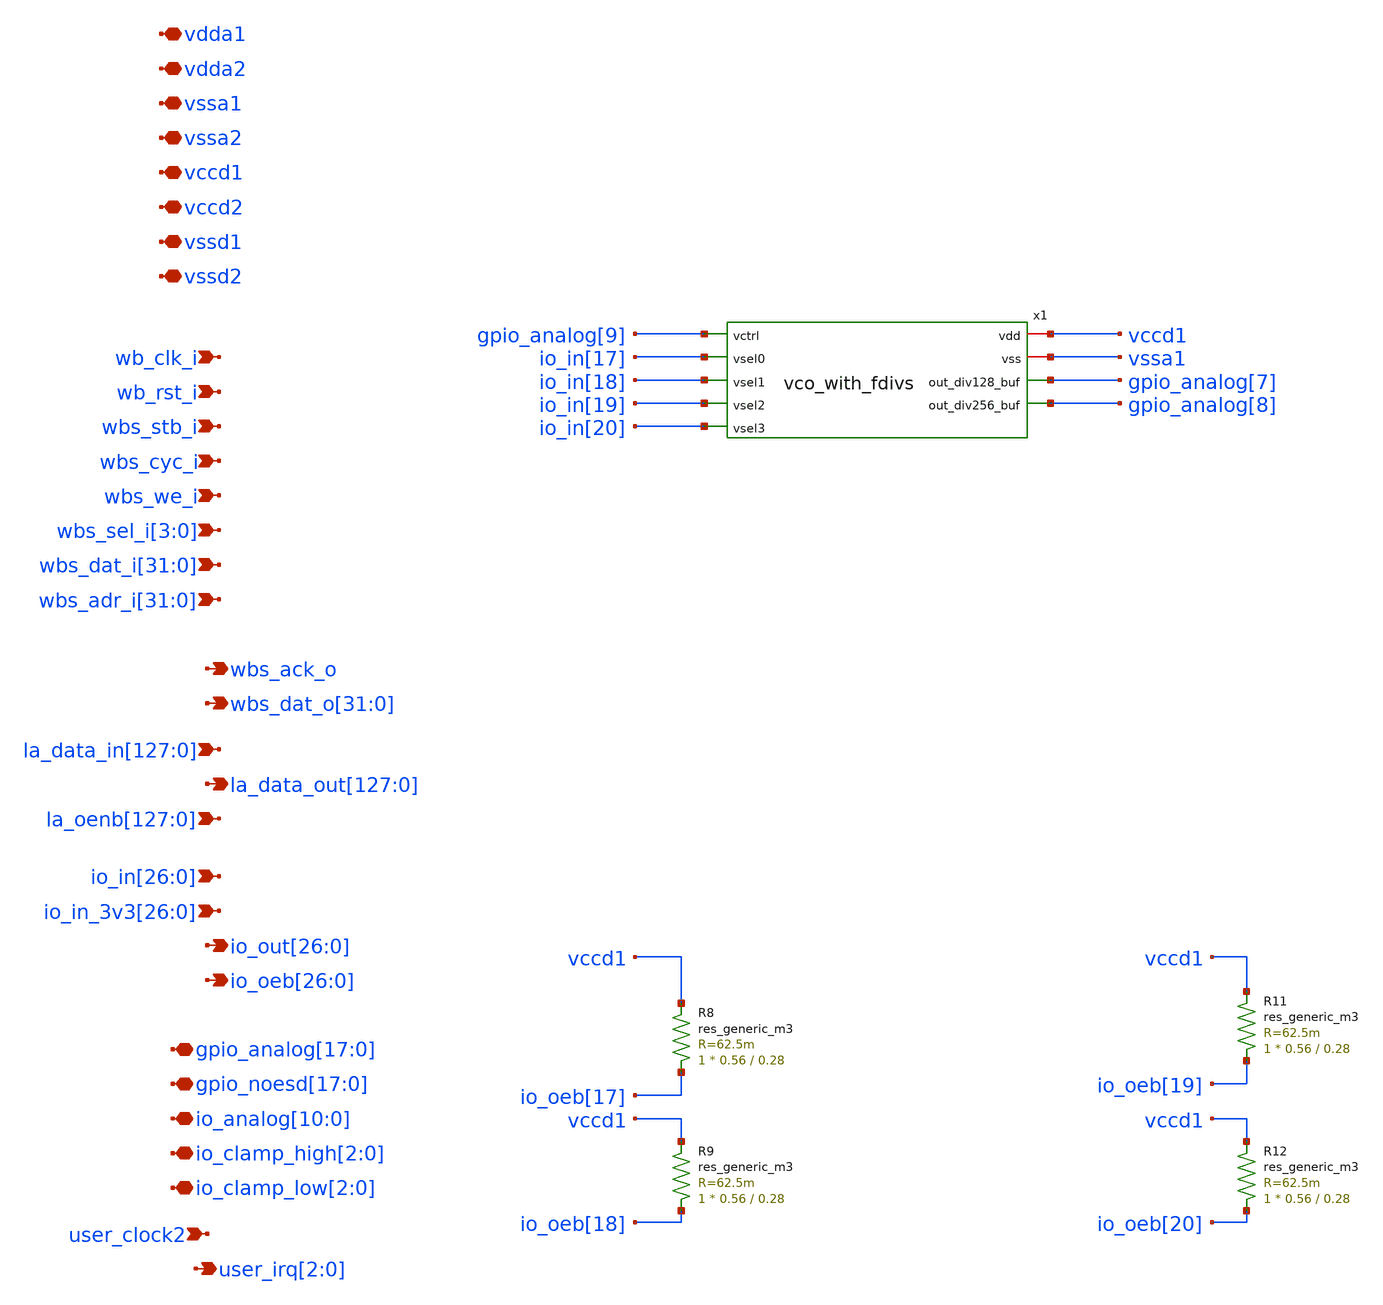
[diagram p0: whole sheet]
** sch_path: xschem/unused/user_analog_project_wrapper_vco_-_seccopy_18-3-2022_10y11.sch
**.subckt user_analog_project_wrapper_vco_-_seccopy_18-3-2022_10y11 vdda1 vdda2 vssa1 vssa2 vccd1
*+ vccd2 vssd1 vssd2 wb_clk_i wb_rst_i wbs_stb_i wbs_cyc_i wbs_we_i
*+ wbs_sel_i[3],wbs_sel_i[2],wbs_sel_i[1],wbs_sel_i[0]
*+ wbs_dat_i[31],wbs_dat_i[30],wbs_dat_i[29],wbs_dat_i[28],wbs_dat_i[27],wbs_dat_i[26],wbs_dat_i[25],wbs_dat_i[24],wbs_dat_i[23],wbs_dat_i[22],wbs_dat_i[21],wbs_dat_i[20],wbs_dat_i[19],wbs_dat_i[18],wbs_dat_i[17],wbs_dat_i[16],wbs_dat_i[15],wbs_dat_i[14],wbs_dat_i[13],wbs_dat_i[12],wbs_dat_i[11],wbs_dat_i[10],wbs_dat_i[9],wbs_dat_i[8],wbs_dat_i[7],wbs_dat_i[6],wbs_dat_i[5],wbs_dat_i[4],wbs_dat_i[3],wbs_dat_i[2],wbs_dat_i[1],wbs_dat_i[0]
*+ wbs_adr_i[31],wbs_adr_i[30],wbs_adr_i[29],wbs_adr_i[28],wbs_adr_i[27],wbs_adr_i[26],wbs_adr_i[25],wbs_adr_i[24],wbs_adr_i[23],wbs_adr_i[22],wbs_adr_i[21],wbs_adr_i[20],wbs_adr_i[19],wbs_adr_i[18],wbs_adr_i[17],wbs_adr_i[16],wbs_adr_i[15],wbs_adr_i[14],wbs_adr_i[13],wbs_adr_i[12],wbs_adr_i[11],wbs_adr_i[10],wbs_adr_i[9],wbs_adr_i[8],wbs_adr_i[7],wbs_adr_i[6],wbs_adr_i[5],wbs_adr_i[4],wbs_adr_i[3],wbs_adr_i[2],wbs_adr_i[1],wbs_adr_i[0] wbs_ack_o
*+ wbs_dat_o[31],wbs_dat_o[30],wbs_dat_o[29],wbs_dat_o[28],wbs_dat_o[27],wbs_dat_o[26],wbs_dat_o[25],wbs_dat_o[24],wbs_dat_o[23],wbs_dat_o[22],wbs_dat_o[21],wbs_dat_o[20],wbs_dat_o[19],wbs_dat_o[18],wbs_dat_o[17],wbs_dat_o[16],wbs_dat_o[15],wbs_dat_o[14],wbs_dat_o[13],wbs_dat_o[12],wbs_dat_o[11],wbs_dat_o[10],wbs_dat_o[9],wbs_dat_o[8],wbs_dat_o[7],wbs_dat_o[6],wbs_dat_o[5],wbs_dat_o[4],wbs_dat_o[3],wbs_dat_o[2],wbs_dat_o[1],wbs_dat_o[0]
*+ la_data_in[127],la_data_in[126],la_data_in[125],la_data_in[124],la_data_in[123],la_data_in[122],la_data_in[121],la_data_in[120],la_data_in[119],la_data_in[118],la_data_in[117],la_data_in[116],la_data_in[115],la_data_in[114],la_data_in[113],la_data_in[112],la_data_in[111],la_data_in[110],la_data_in[109],la_data_in[108],la_data_in[107],la_data_in[106],la_data_in[105],la_data_in[104],la_data_in[103],la_data_in[102],la_data_in[101],la_data_in[100],la_data_in[99],la_data_in[98],la_data_in[97],la_data_in[96],la_data_in[95],la_data_in[94],la_data_in[93],la_data_in[92],la_data_in[91],la_data_in[90],la_data_in[89],la_data_in[88],la_data_in[87],la_data_in[86],la_data_in[85],la_data_in[84],la_data_in[83],la_data_in[82],la_data_in[81],la_data_in[80],la_data_in[79],la_data_in[78],la_data_in[77],la_data_in[76],la_data_in[75],la_data_in[74],la_data_in[73],la_data_in[72],la_data_in[71],la_data_in[70],la_data_in[69],la_data_in[68],la_data_in[67],la_data_in[66],la_data_in[65],la_data_in[64],la_data_in[63],la_data_in[62],la_data_in[61],la_data_in[60],la_data_in[59],la_data_in[58],la_data_in[57],la_data_in[56],la_data_in[55],la_data_in[54],la_data_in[53],la_data_in[52],la_data_in[51],la_data_in[50],la_data_in[49],la_data_in[48],la_data_in[47],la_data_in[46],la_data_in[45],la_data_in[44],la_data_in[43],la_data_in[42],la_data_in[41],la_data_in[40],la_data_in[39],la_data_in[38],la_data_in[37],la_data_in[36],la_data_in[35],la_data_in[34],la_data_in[33],la_data_in[32],la_data_in[31],la_data_in[30],la_data_in[29],la_data_in[28],la_data_in[27],la_data_in[26],la_data_in[25],la_data_in[24],la_data_in[23],la_data_in[22],la_data_in[21],la_data_in[20],la_data_in[19],la_data_in[18],la_data_in[17],la_data_in[16],la_data_in[15],la_data_in[14],la_data_in[13],la_data_in[12],la_data_in[11],la_data_in[10],la_data_in[9],la_data_in[8],la_data_in[7],la_data_in[6],la_data_in[5],la_data_in[4],la_data_in[3],la_data_in[2],la_data_in[1],la_data_in[0]
*+ la_data_out[127],la_data_out[126],la_data_out[125],la_data_out[124],la_data_out[123],la_data_out[122],la_data_out[121],la_data_out[120],la_data_out[119],la_data_out[118],la_data_out[117],la_data_out[116],la_data_out[115],la_data_out[114],la_data_out[113],la_data_out[112],la_data_out[111],la_data_out[110],la_data_out[109],la_data_out[108],la_data_out[107],la_data_out[106],la_data_out[105],la_data_out[104],la_data_out[103],la_data_out[102],la_data_out[101],la_data_out[100],la_data_out[99],la_data_out[98],la_data_out[97],la_data_out[96],la_data_out[95],la_data_out[94],la_data_out[93],la_data_out[92],la_data_out[91],la_data_out[90],la_data_out[89],la_data_out[88],la_data_out[87],la_data_out[86],la_data_out[85],la_data_out[84],la_data_out[83],la_data_out[82],la_data_out[81],la_data_out[80],la_data_out[79],la_data_out[78],la_data_out[77],la_data_out[76],la_data_out[75],la_data_out[74],la_data_out[73],la_data_out[72],la_data_out[71],la_data_out[70],la_data_out[69],la_data_out[68],la_data_out[67],la_data_out[66],la_data_out[65],la_data_out[64],la_data_out[63],la_data_out[62],la_data_out[61],la_data_out[60],la_data_out[59],la_data_out[58],la_data_out[57],la_data_out[56],la_data_out[55],la_data_out[54],la_data_out[53],la_data_out[52],la_data_out[51],la_data_out[50],la_data_out[49],la_data_out[48],la_data_out[47],la_data_out[46],la_data_out[45],la_data_out[44],la_data_out[43],la_data_out[42],la_data_out[41],la_data_out[40],la_data_out[39],la_data_out[38],la_data_out[37],la_data_out[36],la_data_out[35],la_data_out[34],la_data_out[33],la_data_out[32],la_data_out[31],la_data_out[30],la_data_out[29],la_data_out[28],la_data_out[27],la_data_out[26],la_data_out[25],la_data_out[24],la_data_out[23],la_data_out[22],la_data_out[21],la_data_out[20],la_data_out[19],la_data_out[18],la_data_out[17],la_data_out[16],la_data_out[15],la_data_out[14],la_data_out[13],la_data_out[12],la_data_out[11],la_data_out[10],la_data_out[9],la_data_out[8],la_data_out[7],la_data_out[6],la_data_out[5],la_data_out[4],la_data_out[3],la_data_out[2],la_data_out[1],la_data_out[0]
*+ io_in[26],io_in[25],io_in[24],io_in[23],io_in[22],io_in[21],io_in[20],io_in[19],io_in[18],io_in[17],io_in[16],io_in[15],io_in[14],io_in[13],io_in[12],io_in[11],io_in[10],io_in[9],io_in[8],io_in[7],io_in[6],io_in[5],io_in[4],io_in[3],io_in[2],io_in[1],io_in[0]
*+ io_in_3v3[26],io_in_3v3[25],io_in_3v3[24],io_in_3v3[23],io_in_3v3[22],io_in_3v3[21],io_in_3v3[20],io_in_3v3[19],io_in_3v3[18],io_in_3v3[17],io_in_3v3[16],io_in_3v3[15],io_in_3v3[14],io_in_3v3[13],io_in_3v3[12],io_in_3v3[11],io_in_3v3[10],io_in_3v3[9],io_in_3v3[8],io_in_3v3[7],io_in_3v3[6],io_in_3v3[5],io_in_3v3[4],io_in_3v3[3],io_in_3v3[2],io_in_3v3[1],io_in_3v3[0] user_clock2
*+ io_out[26],io_out[25],io_out[24],io_out[23],io_out[22],io_out[21],io_out[20],io_out[19],io_out[18],io_out[17],io_out[16],io_out[15],io_out[14],io_out[13],io_out[12],io_out[11],io_out[10],io_out[9],io_out[8],io_out[7],io_out[6],io_out[5],io_out[4],io_out[3],io_out[2],io_out[1],io_out[0]
*+ io_oeb[26],io_oeb[25],io_oeb[24],io_oeb[23],io_oeb[22],io_oeb[21],io_oeb[20],io_oeb[19],io_oeb[18],io_oeb[17],io_oeb[16],io_oeb[15],io_oeb[14],io_oeb[13],io_oeb[12],io_oeb[11],io_oeb[10],io_oeb[9],io_oeb[8],io_oeb[7],io_oeb[6],io_oeb[5],io_oeb[4],io_oeb[3],io_oeb[2],io_oeb[1],io_oeb[0]
*+ gpio_analog[17],gpio_analog[16],gpio_analog[15],gpio_analog[14],gpio_analog[13],gpio_analog[12],gpio_analog[11],gpio_analog[10],gpio_analog[9],gpio_analog[8],gpio_analog[7],gpio_analog[6],gpio_analog[5],gpio_analog[4],gpio_analog[3],gpio_analog[2],gpio_analog[1],gpio_analog[0]
*+ gpio_noesd[17],gpio_noesd[16],gpio_noesd[15],gpio_noesd[14],gpio_noesd[13],gpio_noesd[12],gpio_noesd[11],gpio_noesd[10],gpio_noesd[9],gpio_noesd[8],gpio_noesd[7],gpio_noesd[6],gpio_noesd[5],gpio_noesd[4],gpio_noesd[3],gpio_noesd[2],gpio_noesd[1],gpio_noesd[0]
*+ io_analog[10],io_analog[9],io_analog[8],io_analog[7],io_analog[6],io_analog[5],io_analog[4],io_analog[3],io_analog[2],io_analog[1],io_analog[0] io_clamp_high[2],io_clamp_high[1],io_clamp_high[0] io_clamp_low[2],io_clamp_low[1],io_clamp_low[0]
*+ user_irq[2],user_irq[1],user_irq[0]
*+ la_oenb[127],la_oenb[126],la_oenb[125],la_oenb[124],la_oenb[123],la_oenb[122],la_oenb[121],la_oenb[120],la_oenb[119],la_oenb[118],la_oenb[117],la_oenb[116],la_oenb[115],la_oenb[114],la_oenb[113],la_oenb[112],la_oenb[111],la_oenb[110],la_oenb[109],la_oenb[108],la_oenb[107],la_oenb[106],la_oenb[105],la_oenb[104],la_oenb[103],la_oenb[102],la_oenb[101],la_oenb[100],la_oenb[99],la_oenb[98],la_oenb[97],la_oenb[96],la_oenb[95],la_oenb[94],la_oenb[93],la_oenb[92],la_oenb[91],la_oenb[90],la_oenb[89],la_oenb[88],la_oenb[87],la_oenb[86],la_oenb[85],la_oenb[84],la_oenb[83],la_oenb[82],la_oenb[81],la_oenb[80],la_oenb[79],la_oenb[78],la_oenb[77],la_oenb[76],la_oenb[75],la_oenb[74],la_oenb[73],la_oenb[72],la_oenb[71],la_oenb[70],la_oenb[69],la_oenb[68],la_oenb[67],la_oenb[66],la_oenb[65],la_oenb[64],la_oenb[63],la_oenb[62],la_oenb[61],la_oenb[60],la_oenb[59],la_oenb[58],la_oenb[57],la_oenb[56],la_oenb[55],la_oenb[54],la_oenb[53],la_oenb[52],la_oenb[51],la_oenb[50],la_oenb[49],la_oenb[48],la_oenb[47],la_oenb[46],la_oenb[45],la_oenb[44],la_oenb[43],la_oenb[42],la_oenb[41],la_oenb[40],la_oenb[39],la_oenb[38],la_oenb[37],la_oenb[36],la_oenb[35],la_oenb[34],la_oenb[33],la_oenb[32],la_oenb[31],la_oenb[30],la_oenb[29],la_oenb[28],la_oenb[27],la_oenb[26],la_oenb[25],la_oenb[24],la_oenb[23],la_oenb[22],la_oenb[21],la_oenb[20],la_oenb[19],la_oenb[18],la_oenb[17],la_oenb[16],la_oenb[15],la_oenb[14],la_oenb[13],la_oenb[12],la_oenb[11],la_oenb[10],la_oenb[9],la_oenb[8],la_oenb[7],la_oenb[6],la_oenb[5],la_oenb[4],la_oenb[3],la_oenb[2],la_oenb[1],la_oenb[0]
*.iopin vdda1
*.iopin vdda2
*.iopin vssa1
*.iopin vssa2
*.iopin vccd1
*.iopin vccd2
*.iopin vssd1
*.iopin vssd2
*.ipin wb_clk_i
*.ipin wb_rst_i
*.ipin wbs_stb_i
*.ipin wbs_cyc_i
*.ipin wbs_we_i
*.ipin wbs_sel_i[3],wbs_sel_i[2],wbs_sel_i[1],wbs_sel_i[0]
*.ipin
*+ wbs_dat_i[31],wbs_dat_i[30],wbs_dat_i[29],wbs_dat_i[28],wbs_dat_i[27],wbs_dat_i[26],wbs_dat_i[25],wbs_dat_i[24],wbs_dat_i[23],wbs_dat_i[22],wbs_dat_i[21],wbs_dat_i[20],wbs_dat_i[19],wbs_dat_i[18],wbs_dat_i[17],wbs_dat_i[16],wbs_dat_i[15],wbs_dat_i[14],wbs_dat_i[13],wbs_dat_i[12],wbs_dat_i[11],wbs_dat_i[10],wbs_dat_i[9],wbs_dat_i[8],wbs_dat_i[7],wbs_dat_i[6],wbs_dat_i[5],wbs_dat_i[4],wbs_dat_i[3],wbs_dat_i[2],wbs_dat_i[1],wbs_dat_i[0]
*.ipin
*+ wbs_adr_i[31],wbs_adr_i[30],wbs_adr_i[29],wbs_adr_i[28],wbs_adr_i[27],wbs_adr_i[26],wbs_adr_i[25],wbs_adr_i[24],wbs_adr_i[23],wbs_adr_i[22],wbs_adr_i[21],wbs_adr_i[20],wbs_adr_i[19],wbs_adr_i[18],wbs_adr_i[17],wbs_adr_i[16],wbs_adr_i[15],wbs_adr_i[14],wbs_adr_i[13],wbs_adr_i[12],wbs_adr_i[11],wbs_adr_i[10],wbs_adr_i[9],wbs_adr_i[8],wbs_adr_i[7],wbs_adr_i[6],wbs_adr_i[5],wbs_adr_i[4],wbs_adr_i[3],wbs_adr_i[2],wbs_adr_i[1],wbs_adr_i[0]
*.opin wbs_ack_o
*.opin
*+ wbs_dat_o[31],wbs_dat_o[30],wbs_dat_o[29],wbs_dat_o[28],wbs_dat_o[27],wbs_dat_o[26],wbs_dat_o[25],wbs_dat_o[24],wbs_dat_o[23],wbs_dat_o[22],wbs_dat_o[21],wbs_dat_o[20],wbs_dat_o[19],wbs_dat_o[18],wbs_dat_o[17],wbs_dat_o[16],wbs_dat_o[15],wbs_dat_o[14],wbs_dat_o[13],wbs_dat_o[12],wbs_dat_o[11],wbs_dat_o[10],wbs_dat_o[9],wbs_dat_o[8],wbs_dat_o[7],wbs_dat_o[6],wbs_dat_o[5],wbs_dat_o[4],wbs_dat_o[3],wbs_dat_o[2],wbs_dat_o[1],wbs_dat_o[0]
*.ipin
*+ la_data_in[127],la_data_in[126],la_data_in[125],la_data_in[124],la_data_in[123],la_data_in[122],la_data_in[121],la_data_in[120],la_data_in[119],la_data_in[118],la_data_in[117],la_data_in[116],la_data_in[115],la_data_in[114],la_data_in[113],la_data_in[112],la_data_in[111],la_data_in[110],la_data_in[109],la_data_in[108],la_data_in[107],la_data_in[106],la_data_in[105],la_data_in[104],la_data_in[103],la_data_in[102],la_data_in[101],la_data_in[100],la_data_in[99],la_data_in[98],la_data_in[97],la_data_in[96],la_data_in[95],la_data_in[94],la_data_in[93],la_data_in[92],la_data_in[91],la_data_in[90],la_data_in[89],la_data_in[88],la_data_in[87],la_data_in[86],la_data_in[85],la_data_in[84],la_data_in[83],la_data_in[82],la_data_in[81],la_data_in[80],la_data_in[79],la_data_in[78],la_data_in[77],la_data_in[76],la_data_in[75],la_data_in[74],la_data_in[73],la_data_in[72],la_data_in[71],la_data_in[70],la_data_in[69],la_data_in[68],la_data_in[67],la_data_in[66],la_data_in[65],la_data_in[64],la_data_in[63],la_data_in[62],la_data_in[61],la_data_in[60],la_data_in[59],la_data_in[58],la_data_in[57],la_data_in[56],la_data_in[55],la_data_in[54],la_data_in[53],la_data_in[52],la_data_in[51],la_data_in[50],la_data_in[49],la_data_in[48],la_data_in[47],la_data_in[46],la_data_in[45],la_data_in[44],la_data_in[43],la_data_in[42],la_data_in[41],la_data_in[40],la_data_in[39],la_data_in[38],la_data_in[37],la_data_in[36],la_data_in[35],la_data_in[34],la_data_in[33],la_data_in[32],la_data_in[31],la_data_in[30],la_data_in[29],la_data_in[28],la_data_in[27],la_data_in[26],la_data_in[25],la_data_in[24],la_data_in[23],la_data_in[22],la_data_in[21],la_data_in[20],la_data_in[19],la_data_in[18],la_data_in[17],la_data_in[16],la_data_in[15],la_data_in[14],la_data_in[13],la_data_in[12],la_data_in[11],la_data_in[10],la_data_in[9],la_data_in[8],la_data_in[7],la_data_in[6],la_data_in[5],la_data_in[4],la_data_in[3],la_data_in[2],la_data_in[1],la_data_in[0]
*.opin
*+ la_data_out[127],la_data_out[126],la_data_out[125],la_data_out[124],la_data_out[123],la_data_out[122],la_data_out[121],la_data_out[120],la_data_out[119],la_data_out[118],la_data_out[117],la_data_out[116],la_data_out[115],la_data_out[114],la_data_out[113],la_data_out[112],la_data_out[111],la_data_out[110],la_data_out[109],la_data_out[108],la_data_out[107],la_data_out[106],la_data_out[105],la_data_out[104],la_data_out[103],la_data_out[102],la_data_out[101],la_data_out[100],la_data_out[99],la_data_out[98],la_data_out[97],la_data_out[96],la_data_out[95],la_data_out[94],la_data_out[93],la_data_out[92],la_data_out[91],la_data_out[90],la_data_out[89],la_data_out[88],la_data_out[87],la_data_out[86],la_data_out[85],la_data_out[84],la_data_out[83],la_data_out[82],la_data_out[81],la_data_out[80],la_data_out[79],la_data_out[78],la_data_out[77],la_data_out[76],la_data_out[75],la_data_out[74],la_data_out[73],la_data_out[72],la_data_out[71],la_data_out[70],la_data_out[69],la_data_out[68],la_data_out[67],la_data_out[66],la_data_out[65],la_data_out[64],la_data_out[63],la_data_out[62],la_data_out[61],la_data_out[60],la_data_out[59],la_data_out[58],la_data_out[57],la_data_out[56],la_data_out[55],la_data_out[54],la_data_out[53],la_data_out[52],la_data_out[51],la_data_out[50],la_data_out[49],la_data_out[48],la_data_out[47],la_data_out[46],la_data_out[45],la_data_out[44],la_data_out[43],la_data_out[42],la_data_out[41],la_data_out[40],la_data_out[39],la_data_out[38],la_data_out[37],la_data_out[36],la_data_out[35],la_data_out[34],la_data_out[33],la_data_out[32],la_data_out[31],la_data_out[30],la_data_out[29],la_data_out[28],la_data_out[27],la_data_out[26],la_data_out[25],la_data_out[24],la_data_out[23],la_data_out[22],la_data_out[21],la_data_out[20],la_data_out[19],la_data_out[18],la_data_out[17],la_data_out[16],la_data_out[15],la_data_out[14],la_data_out[13],la_data_out[12],la_data_out[11],la_data_out[10],la_data_out[9],la_data_out[8],la_data_out[7],la_data_out[6],la_data_out[5],la_data_out[4],la_data_out[3],la_data_out[2],la_data_out[1],la_data_out[0]
*.ipin
*+ io_in[26],io_in[25],io_in[24],io_in[23],io_in[22],io_in[21],io_in[20],io_in[19],io_in[18],io_in[17],io_in[16],io_in[15],io_in[14],io_in[13],io_in[12],io_in[11],io_in[10],io_in[9],io_in[8],io_in[7],io_in[6],io_in[5],io_in[4],io_in[3],io_in[2],io_in[1],io_in[0]
*.ipin
*+ io_in_3v3[26],io_in_3v3[25],io_in_3v3[24],io_in_3v3[23],io_in_3v3[22],io_in_3v3[21],io_in_3v3[20],io_in_3v3[19],io_in_3v3[18],io_in_3v3[17],io_in_3v3[16],io_in_3v3[15],io_in_3v3[14],io_in_3v3[13],io_in_3v3[12],io_in_3v3[11],io_in_3v3[10],io_in_3v3[9],io_in_3v3[8],io_in_3v3[7],io_in_3v3[6],io_in_3v3[5],io_in_3v3[4],io_in_3v3[3],io_in_3v3[2],io_in_3v3[1],io_in_3v3[0]
*.ipin user_clock2
*.opin
*+ io_out[26],io_out[25],io_out[24],io_out[23],io_out[22],io_out[21],io_out[20],io_out[19],io_out[18],io_out[17],io_out[16],io_out[15],io_out[14],io_out[13],io_out[12],io_out[11],io_out[10],io_out[9],io_out[8],io_out[7],io_out[6],io_out[5],io_out[4],io_out[3],io_out[2],io_out[1],io_out[0]
*.opin
*+ io_oeb[26],io_oeb[25],io_oeb[24],io_oeb[23],io_oeb[22],io_oeb[21],io_oeb[20],io_oeb[19],io_oeb[18],io_oeb[17],io_oeb[16],io_oeb[15],io_oeb[14],io_oeb[13],io_oeb[12],io_oeb[11],io_oeb[10],io_oeb[9],io_oeb[8],io_oeb[7],io_oeb[6],io_oeb[5],io_oeb[4],io_oeb[3],io_oeb[2],io_oeb[1],io_oeb[0]
*.iopin
*+ gpio_analog[17],gpio_analog[16],gpio_analog[15],gpio_analog[14],gpio_analog[13],gpio_analog[12],gpio_analog[11],gpio_analog[10],gpio_analog[9],gpio_analog[8],gpio_analog[7],gpio_analog[6],gpio_analog[5],gpio_analog[4],gpio_analog[3],gpio_analog[2],gpio_analog[1],gpio_analog[0]
*.iopin
*+ gpio_noesd[17],gpio_noesd[16],gpio_noesd[15],gpio_noesd[14],gpio_noesd[13],gpio_noesd[12],gpio_noesd[11],gpio_noesd[10],gpio_noesd[9],gpio_noesd[8],gpio_noesd[7],gpio_noesd[6],gpio_noesd[5],gpio_noesd[4],gpio_noesd[3],gpio_noesd[2],gpio_noesd[1],gpio_noesd[0]
*.iopin
*+ io_analog[10],io_analog[9],io_analog[8],io_analog[7],io_analog[6],io_analog[5],io_analog[4],io_analog[3],io_analog[2],io_analog[1],io_analog[0]
*.iopin io_clamp_high[2],io_clamp_high[1],io_clamp_high[0]
*.iopin io_clamp_low[2],io_clamp_low[1],io_clamp_low[0]
*.opin user_irq[2],user_irq[1],user_irq[0]
*.ipin
*+ la_oenb[127],la_oenb[126],la_oenb[125],la_oenb[124],la_oenb[123],la_oenb[122],la_oenb[121],la_oenb[120],la_oenb[119],la_oenb[118],la_oenb[117],la_oenb[116],la_oenb[115],la_oenb[114],la_oenb[113],la_oenb[112],la_oenb[111],la_oenb[110],la_oenb[109],la_oenb[108],la_oenb[107],la_oenb[106],la_oenb[105],la_oenb[104],la_oenb[103],la_oenb[102],la_oenb[101],la_oenb[100],la_oenb[99],la_oenb[98],la_oenb[97],la_oenb[96],la_oenb[95],la_oenb[94],la_oenb[93],la_oenb[92],la_oenb[91],la_oenb[90],la_oenb[89],la_oenb[88],la_oenb[87],la_oenb[86],la_oenb[85],la_oenb[84],la_oenb[83],la_oenb[82],la_oenb[81],la_oenb[80],la_oenb[79],la_oenb[78],la_oenb[77],la_oenb[76],la_oenb[75],la_oenb[74],la_oenb[73],la_oenb[72],la_oenb[71],la_oenb[70],la_oenb[69],la_oenb[68],la_oenb[67],la_oenb[66],la_oenb[65],la_oenb[64],la_oenb[63],la_oenb[62],la_oenb[61],la_oenb[60],la_oenb[59],la_oenb[58],la_oenb[57],la_oenb[56],la_oenb[55],la_oenb[54],la_oenb[53],la_oenb[52],la_oenb[51],la_oenb[50],la_oenb[49],la_oenb[48],la_oenb[47],la_oenb[46],la_oenb[45],la_oenb[44],la_oenb[43],la_oenb[42],la_oenb[41],la_oenb[40],la_oenb[39],la_oenb[38],la_oenb[37],la_oenb[36],la_oenb[35],la_oenb[34],la_oenb[33],la_oenb[32],la_oenb[31],la_oenb[30],la_oenb[29],la_oenb[28],la_oenb[27],la_oenb[26],la_oenb[25],la_oenb[24],la_oenb[23],la_oenb[22],la_oenb[21],la_oenb[20],la_oenb[19],la_oenb[18],la_oenb[17],la_oenb[16],la_oenb[15],la_oenb[14],la_oenb[13],la_oenb[12],la_oenb[11],la_oenb[10],la_oenb[9],la_oenb[8],la_oenb[7],la_oenb[6],la_oenb[5],la_oenb[4],la_oenb[3],la_oenb[2],la_oenb[1],la_oenb[0]
R8 io_oeb[17] vccd1 sky130_fd_pr__res_generic_m3 W=0.56 L=0.28 m=1
R9 io_oeb[18] vccd1 sky130_fd_pr__res_generic_m3 W=0.56 L=0.28 m=1
R11 io_oeb[19] vccd1 sky130_fd_pr__res_generic_m3 W=0.56 L=0.28 m=1
R12 io_oeb[20] vccd1 sky130_fd_pr__res_generic_m3 W=0.56 L=0.28 m=1
x1 vccd1 gpio_analog[9] io_in[17] io_in[18] io_in[19] io_in[20] vssa1 gpio_analog[7] gpio_analog[8]
+ vco_with_fdivs
**.ends

* expanding   symbol:
*+  /home/darunixspro3/Desktop/GitSandboxes/VCO_spro3/VCO_-_seccopy_16-3-2022_11y40/vco/xschem/vco_with_fdivs.sym # of pins=9
** sym_path: xschem/3-stage_cs-vco_dp9/vco_with_fdivs.sym
** sch_path: xschem/3-stage_cs-vco_dp9/vco_with_fdivs.sch
.subckt vco_with_fdivs vdd vctrl vsel0 vsel1 vsel2 vsel3 vss out_div128_buf out_div256_buf
*.ipin vctrl
*.opin out_div128_buf
*.iopin vdd
*.iopin vss
*.ipin vsel0
*.ipin vsel1
*.ipin vsel2
*.ipin vsel3
*.opin out_div256_buf
xvco vdd out vctrl vss vsel0 vsel1 vsel2 vsel3 3-stage_cs-vco_dp9
xFD_0 vdd out_div2 vss out FD_v5
xbuf2a out_div128 vss vss vdd vdd buf2a_out sky130_fd_sc_hd__clkbuf_2
xbuf4a buf2a_out vss vss vdd vdd buf4a_out sky130_fd_sc_hd__clkbuf_4
xbuf8a buf4a_out vss vss vdd vdd buf8a_out sky130_fd_sc_hd__clkbuf_8
xFD_1 vdd out_div4 vss out_div2 FD
xFD_2 vdd out_div8 vss out_div4 FD
xFD_3 vdd out_div16 vss out_div8 FD
xFD_4 vdd out_div32 vss out_div16 FD
xFD_5 vdd out_div64 vss out_div32 FD
xFD_6 vdd out_div128 vss out_div64 FD
xFD_7 vdd out_div256 vss out_div128 FD
xbuf2b out_div256 vss vss vdd vdd buf2b_out sky130_fd_sc_hd__clkbuf_2
xbuf4b buf2b_out vss vss vdd vdd buf4b_out sky130_fd_sc_hd__clkbuf_4
xbuf8b buf4b_out vss vss vdd vdd buf8b_out sky130_fd_sc_hd__clkbuf_8
xFD_8 vdd out_div512 vss out_div256 FD
xFD_9 vdd out_div1024 vss out_div512 FD
xbuf16a buf8a_out vss vss vdd vdd buf16a_out sky130_fd_sc_hd__clkbuf_16
xbuf16b buf8b_out vss vss vdd vdd out_div256_buf sky130_fd_sc_hd__clkbuf_16
xbuf32a_1 buf16a_out vss vss vdd vdd out_div128_buf sky130_fd_sc_hd__clkbuf_16
xbuf32a_2 buf16a_out vss vss vdd vdd out_div128_buf sky130_fd_sc_hd__clkbuf_16
.ends


* expanding   symbol:  3-stage_cs-vco_dp9.sym # of pins=8
** sym_path: xschem/3-stage_cs-vco_dp9/3-stage_cs-vco_dp9.sym
** sch_path: xschem/3-stage_cs-vco_dp9/3-stage_cs-vco_dp9.sch
.subckt 3-stage_cs-vco_dp9 vdd out vctrl vss sel0 sel1 sel2 sel3
*.iopin vdd
*.iopin vss
*.opin out
*.ipin vctrl
*.ipin sel0
*.ipin sel1
*.ipin sel2
*.ipin sel3
XM25 vgp vgp vdd vdd sky130_fd_pr__pfet_01v8 L=0.18 W=1 nf=1 ad='int((nf+1)/2) * W/nf * 0.29' as='int((nf+2)/2) * W/nf * 0.29'
+ pd='2*int((nf+1)/2) * (W/nf + 0.29)' ps='2*int((nf+2)/2) * (W/nf + 0.29)' nrd='0.29 / W' nrs='0.29 / W'
+ sa=0 sb=0 sd=0 mult=1 m=1
XM26 vgp vctrl vss vss sky130_fd_pr__nfet_01v8 L=0.18 W=1 nf=1 ad='int((nf+1)/2) * W/nf * 0.29' as='int((nf+2)/2) * W/nf * 0.29'
+ pd='2*int((nf+1)/2) * (W/nf + 0.29)' ps='2*int((nf+2)/2) * (W/nf + 0.29)' nrd='0.29 / W' nrs='0.29 / W'
+ sa=0 sb=0 sd=0 mult=1 m=1
XM11C net2 pg2 vdd vdd sky130_fd_pr__pfet_01v8 L=0.18 W=2.4 nf=1 ad='int((nf+1)/2) * W/nf * 0.29' as='int((nf+2)/2) * W/nf * 0.29'
+ pd='2*int((nf+1)/2) * (W/nf + 0.29)' ps='2*int((nf+2)/2) * (W/nf + 0.29)' nrd='0.29 / W' nrs='0.29 / W'
+ sa=0 sb=0 sd=0 mult=1 m=1
XM16A net8 ng0 vss vss sky130_fd_pr__nfet_01v8 L=0.18 W=0.6 nf=1 ad='int((nf+1)/2) * W/nf * 0.29' as='int((nf+2)/2) * W/nf * 0.29'
+ pd='2*int((nf+1)/2) * (W/nf + 0.29)' ps='2*int((nf+2)/2) * (W/nf + 0.29)' nrd='0.29 / W' nrs='0.29 / W'
+ sa=0 sb=0 sd=0 mult=1 m=1
XM1 net3 net5 net2 vdd sky130_fd_pr__pfet_01v8 L=0.15 W=1.4 nf=1 ad='int((nf+1)/2) * W/nf * 0.29' as='int((nf+2)/2) * W/nf * 0.29'
+ pd='2*int((nf+1)/2) * (W/nf + 0.29)' ps='2*int((nf+2)/2) * (W/nf + 0.29)' nrd='0.29 / W' nrs='0.29 / W'
+ sa=0 sb=0 sd=0 mult=1 m=1
XM3 net4 net3 vdd vdd sky130_fd_pr__pfet_01v8 L=0.15 W=0.75 nf=1 ad='int((nf+1)/2) * W/nf * 0.29' as='int((nf+2)/2) * W/nf * 0.29'
+ pd='2*int((nf+1)/2) * (W/nf + 0.29)' ps='2*int((nf+2)/2) * (W/nf + 0.29)' nrd='0.29 / W' nrs='0.29 / W'
+ sa=0 sb=0 sd=0 mult=1 m=1
XM5 net5 net4 vdd vdd sky130_fd_pr__pfet_01v8 L=0.15 W=3 nf=1 ad='int((nf+1)/2) * W/nf * 0.29' as='int((nf+2)/2) * W/nf * 0.29'
+ pd='2*int((nf+1)/2) * (W/nf + 0.29)' ps='2*int((nf+2)/2) * (W/nf + 0.29)' nrd='0.29 / W' nrs='0.29 / W'
+ sa=0 sb=0 sd=0 mult=1 m=1
XM2 net3 net5 net8 vss sky130_fd_pr__nfet_01v8 L=0.15 W=0.72 nf=1 ad='int((nf+1)/2) * W/nf * 0.29' as='int((nf+2)/2) * W/nf * 0.29'
+ pd='2*int((nf+1)/2) * (W/nf + 0.29)' ps='2*int((nf+2)/2) * (W/nf + 0.29)' nrd='0.29 / W' nrs='0.29 / W'
+ sa=0 sb=0 sd=0 mult=1 m=1
XM4 net4 net3 vss vss sky130_fd_pr__nfet_01v8 L=0.15 W=0.5 nf=1 ad='int((nf+1)/2) * W/nf * 0.29' as='int((nf+2)/2) * W/nf * 0.29'
+ pd='2*int((nf+1)/2) * (W/nf + 0.29)' ps='2*int((nf+2)/2) * (W/nf + 0.29)' nrd='0.29 / W' nrs='0.29 / W'
+ sa=0 sb=0 sd=0 mult=1 m=1
XM6 net5 net4 vss vss sky130_fd_pr__nfet_01v8 L=0.15 W=1.44 nf=1 ad='int((nf+1)/2) * W/nf * 0.29' as='int((nf+2)/2) * W/nf * 0.29'
+ pd='2*int((nf+1)/2) * (W/nf + 0.29)' ps='2*int((nf+2)/2) * (W/nf + 0.29)' nrd='0.29 / W' nrs='0.29 / W'
+ sa=0 sb=0 sd=0 mult=1 m=1
XM21 net6 net5 vdd vdd sky130_fd_pr__pfet_01v8 L=0.15 W=0.8 nf=1 ad='int((nf+1)/2) * W/nf * 0.29' as='int((nf+2)/2) * W/nf * 0.29'
+ pd='2*int((nf+1)/2) * (W/nf + 0.29)' ps='2*int((nf+2)/2) * (W/nf + 0.29)' nrd='0.29 / W' nrs='0.29 / W'
+ sa=0 sb=0 sd=0 mult=1 m=1
XM22 net6 net5 vss vss sky130_fd_pr__nfet_01v8 L=0.15 W=0.42 nf=1 ad='int((nf+1)/2) * W/nf * 0.29' as='int((nf+2)/2) * W/nf * 0.29'
+ pd='2*int((nf+1)/2) * (W/nf + 0.29)' ps='2*int((nf+2)/2) * (W/nf + 0.29)' nrd='0.29 / W' nrs='0.29 / W'
+ sa=0 sb=0 sd=0 mult=1 m=1
XM23 out net7 vdd vdd sky130_fd_pr__pfet_01v8 L=0.18 W=6.6 nf=3 ad='int((nf+1)/2) * W/nf * 0.29' as='int((nf+2)/2) * W/nf * 0.29'
+ pd='2*int((nf+1)/2) * (W/nf + 0.29)' ps='2*int((nf+2)/2) * (W/nf + 0.29)' nrd='0.29 / W' nrs='0.29 / W'
+ sa=0 sb=0 sd=0 mult=1 m=1
XM24 out net7 vss vss sky130_fd_pr__nfet_01v8 L=0.18 W=1.29 nf=1 ad='int((nf+1)/2) * W/nf * 0.29' as='int((nf+2)/2) * W/nf * 0.29'
+ pd='2*int((nf+1)/2) * (W/nf + 0.29)' ps='2*int((nf+2)/2) * (W/nf + 0.29)' nrd='0.29 / W' nrs='0.29 / W'
+ sa=0 sb=0 sd=0 mult=1 m=1
XM12 net7 net6 vdd vdd sky130_fd_pr__pfet_01v8 L=0.15 W=2.4 nf=1 ad='int((nf+1)/2) * W/nf * 0.29' as='int((nf+2)/2) * W/nf * 0.29'
+ pd='2*int((nf+1)/2) * (W/nf + 0.29)' ps='2*int((nf+2)/2) * (W/nf + 0.29)' nrd='0.29 / W' nrs='0.29 / W'
+ sa=0 sb=0 sd=0 mult=1 m=1
XM13 net7 net6 vss vss sky130_fd_pr__nfet_01v8 L=0.15 W=1.2 nf=1 ad='int((nf+1)/2) * W/nf * 0.29' as='int((nf+2)/2) * W/nf * 0.29'
+ pd='2*int((nf+1)/2) * (W/nf + 0.29)' ps='2*int((nf+2)/2) * (W/nf + 0.29)' nrd='0.29 / W' nrs='0.29 / W'
+ sa=0 sb=0 sd=0 mult=1 m=1
XMDUM16B vss vss vss vss sky130_fd_pr__nfet_01v8 L=0.18 W=2.4 nf=1 ad='int((nf+1)/2) * W/nf * 0.29' as='int((nf+2)/2) * W/nf * 0.29'
+ pd='2*int((nf+1)/2) * (W/nf + 0.29)' ps='2*int((nf+2)/2) * (W/nf + 0.29)' nrd='0.29 / W' nrs='0.29 / W'
+ sa=0 sb=0 sd=0 mult=1 m=1
XMDUM16 vss vss vss vss sky130_fd_pr__nfet_01v8 L=0.18 W=2.4 nf=1 ad='int((nf+1)/2) * W/nf * 0.29' as='int((nf+2)/2) * W/nf * 0.29'
+ pd='2*int((nf+1)/2) * (W/nf + 0.29)' ps='2*int((nf+2)/2) * (W/nf + 0.29)' nrd='0.29 / W' nrs='0.29 / W'
+ sa=0 sb=0 sd=0 mult=1 m=1
XMDUM26 vss vss vss vss sky130_fd_pr__nfet_01v8 L=0.18 W=1 nf=1 ad='int((nf+1)/2) * W/nf * 0.29' as='int((nf+2)/2) * W/nf * 0.29'
+ pd='2*int((nf+1)/2) * (W/nf + 0.29)' ps='2*int((nf+2)/2) * (W/nf + 0.29)' nrd='0.29 / W' nrs='0.29 / W'
+ sa=0 sb=0 sd=0 mult=1 m=1
XMDUM11B vdd vdd vdd vdd sky130_fd_pr__pfet_01v8 L=0.18 W=2.4 nf=1 ad='int((nf+1)/2) * W/nf * 0.29' as='int((nf+2)/2) * W/nf * 0.29'
+ pd='2*int((nf+1)/2) * (W/nf + 0.29)' ps='2*int((nf+2)/2) * (W/nf + 0.29)' nrd='0.29 / W' nrs='0.29 / W'
+ sa=0 sb=0 sd=0 mult=1 m=1
XMDUM11 vdd vdd vdd vdd sky130_fd_pr__pfet_01v8 L=0.18 W=2.4 nf=1 ad='int((nf+1)/2) * W/nf * 0.29' as='int((nf+2)/2) * W/nf * 0.29'
+ pd='2*int((nf+1)/2) * (W/nf + 0.29)' ps='2*int((nf+2)/2) * (W/nf + 0.29)' nrd='0.29 / W' nrs='0.29 / W'
+ sa=0 sb=0 sd=0 mult=1 m=1
XMDUM25 vdd vdd vdd vdd sky130_fd_pr__pfet_01v8 L=0.18 W=1 nf=1 ad='int((nf+1)/2) * W/nf * 0.29' as='int((nf+2)/2) * W/nf * 0.29'
+ pd='2*int((nf+1)/2) * (W/nf + 0.29)' ps='2*int((nf+2)/2) * (W/nf + 0.29)' nrd='0.29 / W' nrs='0.29 / W'
+ sa=0 sb=0 sd=0 mult=1 m=1
Cnet8 net3 vss 0.87f m=1
Cnet9 net4 vss 1.14f m=1
Cnet10 net5 vss 3.49f m=1
XMDUM26B vss vss vss vss sky130_fd_pr__nfet_01v8 L=0.18 W=1 nf=1 ad='int((nf+1)/2) * W/nf * 0.29' as='int((nf+2)/2) * W/nf * 0.29'
+ pd='2*int((nf+1)/2) * (W/nf + 0.29)' ps='2*int((nf+2)/2) * (W/nf + 0.29)' nrd='0.29 / W' nrs='0.29 / W'
+ sa=0 sb=0 sd=0 mult=1 m=1
XMDUM25B vdd vdd vdd vdd sky130_fd_pr__pfet_01v8 L=0.18 W=1 nf=1 ad='int((nf+1)/2) * W/nf * 0.29' as='int((nf+2)/2) * W/nf * 0.29'
+ pd='2*int((nf+1)/2) * (W/nf + 0.29)' ps='2*int((nf+2)/2) * (W/nf + 0.29)' nrd='0.29 / W' nrs='0.29 / W'
+ sa=0 sb=0 sd=0 mult=1 m=1
x1n vdd ng0 vctrl vss sel0 vco_switch_n
XM16B net8 ng1 vss vss sky130_fd_pr__nfet_01v8 L=0.18 W=1.2 nf=1 ad='int((nf+1)/2) * W/nf * 0.29' as='int((nf+2)/2) * W/nf * 0.29'
+ pd='2*int((nf+1)/2) * (W/nf + 0.29)' ps='2*int((nf+2)/2) * (W/nf + 0.29)' nrd='0.29 / W' nrs='0.29 / W'
+ sa=0 sb=0 sd=0 mult=1 m=1
x2n vdd ng1 vctrl vss sel1 vco_switch_n
XM16C net8 ng2 vss vss sky130_fd_pr__nfet_01v8 L=0.18 W=2.4 nf=1 ad='int((nf+1)/2) * W/nf * 0.29' as='int((nf+2)/2) * W/nf * 0.29'
+ pd='2*int((nf+1)/2) * (W/nf + 0.29)' ps='2*int((nf+2)/2) * (W/nf + 0.29)' nrd='0.29 / W' nrs='0.29 / W'
+ sa=0 sb=0 sd=0 mult=1 m=1
x3n vdd ng2 vctrl vss sel2 vco_switch_n
XM16D net8 ng3 vss vss sky130_fd_pr__nfet_01v8 L=0.18 W=2.4 nf=1 ad='int((nf+1)/2) * W/nf * 0.29' as='int((nf+2)/2) * W/nf * 0.29'
+ pd='2*int((nf+1)/2) * (W/nf + 0.29)' ps='2*int((nf+2)/2) * (W/nf + 0.29)' nrd='0.29 / W' nrs='0.29 / W'
+ sa=0 sb=0 sd=0 mult=2 m=2
x4n vdd ng3 vctrl vss sel3 vco_switch_n
x3p vdd pg2 vgp vss sel2 vco_switch_p
XM11D net2 pg3 vdd vdd sky130_fd_pr__pfet_01v8 L=0.18 W=2.4 nf=1 ad='int((nf+1)/2) * W/nf * 0.29' as='int((nf+2)/2) * W/nf * 0.29'
+ pd='2*int((nf+1)/2) * (W/nf + 0.29)' ps='2*int((nf+2)/2) * (W/nf + 0.29)' nrd='0.29 / W' nrs='0.29 / W'
+ sa=0 sb=0 sd=0 mult=2 m=2
x4p vdd pg3 vgp vss sel3 vco_switch_p
XM11B net2 pg1 vdd vdd sky130_fd_pr__pfet_01v8 L=0.18 W=1.2 nf=1 ad='int((nf+1)/2) * W/nf * 0.29' as='int((nf+2)/2) * W/nf * 0.29'
+ pd='2*int((nf+1)/2) * (W/nf + 0.29)' ps='2*int((nf+2)/2) * (W/nf + 0.29)' nrd='0.29 / W' nrs='0.29 / W'
+ sa=0 sb=0 sd=0 mult=1 m=1
x2p vdd pg1 vgp vss sel1 vco_switch_p
XM11A net2 pg0 vdd vdd sky130_fd_pr__pfet_01v8 L=0.18 W=0.6 nf=1 ad='int((nf+1)/2) * W/nf * 0.29' as='int((nf+2)/2) * W/nf * 0.29'
+ pd='2*int((nf+1)/2) * (W/nf + 0.29)' ps='2*int((nf+2)/2) * (W/nf + 0.29)' nrd='0.29 / W' nrs='0.29 / W'
+ sa=0 sb=0 sd=0 mult=1 m=1
x1p vdd pg0 vgp vss sel0 vco_switch_p
XM16 net8 vctrl vss vss sky130_fd_pr__nfet_01v8 L=0.18 W=0.6 nf=1 ad='int((nf+1)/2) * W/nf * 0.29' as='int((nf+2)/2) * W/nf * 0.29'
+ pd='2*int((nf+1)/2) * (W/nf + 0.29)' ps='2*int((nf+2)/2) * (W/nf + 0.29)' nrd='0.29 / W' nrs='0.29 / W'
+ sa=0 sb=0 sd=0 mult=1 m=1
XM11 net2 vgp vdd vdd sky130_fd_pr__pfet_01v8 L=0.18 W=0.6 nf=1 ad='int((nf+1)/2) * W/nf * 0.29' as='int((nf+2)/2) * W/nf * 0.29'
+ pd='2*int((nf+1)/2) * (W/nf + 0.29)' ps='2*int((nf+2)/2) * (W/nf + 0.29)' nrd='0.29 / W' nrs='0.29 / W'
+ sa=0 sb=0 sd=0 mult=1 m=1
.ends


* expanding   symbol:  FD_v5.sym # of pins=4
** sym_path: xschem/3-stage_cs-vco_dp9/FD_v5.sym
** sch_path: xschem/3-stage_cs-vco_dp9/FD_v5.sch
.subckt FD_v5 VDD Clk_Out GND Clk_In
*.ipin Clk_In
*.iopin VDD
*.iopin GND
*.opin Clk_Out
XMPbuf1 7 6 VDD VDD sky130_fd_pr__pfet_01v8 L=0.15 W=1.44 nf=1 ad='int((nf+1)/2) * W/nf * 0.29' as='int((nf+2)/2) * W/nf * 0.29'
+ pd='2*int((nf+1)/2) * (W/nf + 0.29)' ps='2*int((nf+2)/2) * (W/nf + 0.29)' nrd='0.29 / W' nrs='0.29 / W'
+ sa=0 sb=0 sd=0 mult=1 m=1
XMNbuf1 7 6 GND GND sky130_fd_pr__nfet_01v8 L=0.15 W=0.84 nf=1 ad='int((nf+1)/2) * W/nf * 0.29' as='int((nf+2)/2) * W/nf * 0.29'
+ pd='2*int((nf+1)/2) * (W/nf + 0.29)' ps='2*int((nf+2)/2) * (W/nf + 0.29)' nrd='0.29 / W' nrs='0.29 / W'
+ sa=0 sb=0 sd=0 mult=1 m=1
XMPClkin Clk_In_buf Clkb_buf VDD VDD sky130_fd_pr__pfet_01v8 L=0.15 W=1.44 nf=1 ad='int((nf+1)/2) * W/nf * 0.29'
+ as='int((nf+2)/2) * W/nf * 0.29' pd='2*int((nf+1)/2) * (W/nf + 0.29)' ps='2*int((nf+2)/2) * (W/nf + 0.29)'
+ nrd='0.29 / W' nrs='0.29 / W' sa=0 sb=0 sd=0 mult=4 m=4
XMNClkin Clk_In_buf Clkb_buf GND GND sky130_fd_pr__nfet_01v8 L=0.15 W=0.84 nf=1 ad='int((nf+1)/2) * W/nf * 0.29'
+ as='int((nf+2)/2) * W/nf * 0.29' pd='2*int((nf+1)/2) * (W/nf + 0.29)' ps='2*int((nf+2)/2) * (W/nf + 0.29)'
+ nrd='0.29 / W' nrs='0.29 / W' sa=0 sb=0 sd=0 mult=3 m=3
XMPinv2 5 4 VDD VDD sky130_fd_pr__pfet_01v8 L=0.15 W=1.44 nf=1 ad='int((nf+1)/2) * W/nf * 0.29' as='int((nf+2)/2) * W/nf * 0.29'
+ pd='2*int((nf+1)/2) * (W/nf + 0.29)' ps='2*int((nf+2)/2) * (W/nf + 0.29)' nrd='0.29 / W' nrs='0.29 / W'
+ sa=0 sb=0 sd=0 mult=4 m=4
XMNinv2 5 4 GND GND sky130_fd_pr__nfet_01v8 L=0.15 W=0.84 nf=1 ad='int((nf+1)/2) * W/nf * 0.29' as='int((nf+2)/2) * W/nf * 0.29'
+ pd='2*int((nf+1)/2) * (W/nf + 0.29)' ps='2*int((nf+2)/2) * (W/nf + 0.29)' nrd='0.29 / W' nrs='0.29 / W'
+ sa=0 sb=0 sd=0 mult=3 m=3
XMPinv1 3 2 VDD VDD sky130_fd_pr__pfet_01v8 L=0.15 W=1.44 nf=1 ad='int((nf+1)/2) * W/nf * 0.29' as='int((nf+2)/2) * W/nf * 0.29'
+ pd='2*int((nf+1)/2) * (W/nf + 0.29)' ps='2*int((nf+2)/2) * (W/nf + 0.29)' nrd='0.29 / W' nrs='0.29 / W'
+ sa=0 sb=0 sd=0 mult=4 m=4
XMNinv1 3 2 GND GND sky130_fd_pr__nfet_01v8 L=0.15 W=0.84 nf=1 ad='int((nf+1)/2) * W/nf * 0.29' as='int((nf+2)/2) * W/nf * 0.29'
+ pd='2*int((nf+1)/2) * (W/nf + 0.29)' ps='2*int((nf+2)/2) * (W/nf + 0.29)' nrd='0.29 / W' nrs='0.29 / W'
+ sa=0 sb=0 sd=0 mult=3 m=3
XMPTgate1 4 Clkb_buf 3 VDD sky130_fd_pr__pfet_01v8 L=0.15 W=1.44 nf=1 ad='int((nf+1)/2) * W/nf * 0.29'
+ as='int((nf+2)/2) * W/nf * 0.29' pd='2*int((nf+1)/2) * (W/nf + 0.29)' ps='2*int((nf+2)/2) * (W/nf + 0.29)'
+ nrd='0.29 / W' nrs='0.29 / W' sa=0 sb=0 sd=0 mult=5 m=5
XMNTgate1 4 Clk_In_buf 3 GND sky130_fd_pr__nfet_01v8 L=0.15 W=0.84 nf=1 ad='int((nf+1)/2) * W/nf * 0.29'
+ as='int((nf+2)/2) * W/nf * 0.29' pd='2*int((nf+1)/2) * (W/nf + 0.29)' ps='2*int((nf+2)/2) * (W/nf + 0.29)'
+ nrd='0.29 / W' nrs='0.29 / W' sa=0 sb=0 sd=0 mult=8 m=8
XMPTgate2 6 Clk_In_buf 5 VDD sky130_fd_pr__pfet_01v8 L=0.15 W=1.44 nf=1 ad='int((nf+1)/2) * W/nf * 0.29'
+ as='int((nf+2)/2) * W/nf * 0.29' pd='2*int((nf+1)/2) * (W/nf + 0.29)' ps='2*int((nf+2)/2) * (W/nf + 0.29)'
+ nrd='0.29 / W' nrs='0.29 / W' sa=0 sb=0 sd=0 mult=5 m=5
XMNTgate2 6 Clkb_buf 5 GND sky130_fd_pr__nfet_01v8 L=0.15 W=0.84 nf=1 ad='int((nf+1)/2) * W/nf * 0.29'
+ as='int((nf+2)/2) * W/nf * 0.29' pd='2*int((nf+1)/2) * (W/nf + 0.29)' ps='2*int((nf+2)/2) * (W/nf + 0.29)'
+ nrd='0.29 / W' nrs='0.29 / W' sa=0 sb=0 sd=0 mult=8 m=8
XMPbuf2 Clk_Out 7 VDD VDD sky130_fd_pr__pfet_01v8 L=0.15 W=1.44 nf=1 ad='int((nf+1)/2) * W/nf * 0.29'
+ as='int((nf+2)/2) * W/nf * 0.29' pd='2*int((nf+1)/2) * (W/nf + 0.29)' ps='2*int((nf+2)/2) * (W/nf + 0.29)'
+ nrd='0.29 / W' nrs='0.29 / W' sa=0 sb=0 sd=0 mult=2 m=2
XMNbuf2 Clk_Out 7 GND GND sky130_fd_pr__nfet_01v8 L=0.15 W=0.84 nf=1 ad='int((nf+1)/2) * W/nf * 0.29'
+ as='int((nf+2)/2) * W/nf * 0.29' pd='2*int((nf+1)/2) * (W/nf + 0.29)' ps='2*int((nf+2)/2) * (W/nf + 0.29)'
+ nrd='0.29 / W' nrs='0.29 / W' sa=0 sb=0 sd=0 mult=2 m=2
XMPfb 2 6 VDD VDD sky130_fd_pr__pfet_01v8 L=0.15 W=1.44 nf=1 ad='int((nf+1)/2) * W/nf * 0.29' as='int((nf+2)/2) * W/nf * 0.29'
+ pd='2*int((nf+1)/2) * (W/nf + 0.29)' ps='2*int((nf+2)/2) * (W/nf + 0.29)' nrd='0.29 / W' nrs='0.29 / W'
+ sa=0 sb=0 sd=0 mult=4 m=4
XMNfb 2 6 GND GND sky130_fd_pr__nfet_01v8 L=0.15 W=0.84 nf=1 ad='int((nf+1)/2) * W/nf * 0.29' as='int((nf+2)/2) * W/nf * 0.29'
+ pd='2*int((nf+1)/2) * (W/nf + 0.29)' ps='2*int((nf+2)/2) * (W/nf + 0.29)' nrd='0.29 / W' nrs='0.29 / W'
+ sa=0 sb=0 sd=0 mult=3 m=3
XMPClkin_b2 net1 Clkb_int VDD VDD sky130_fd_pr__pfet_01v8 L=0.15 W=1.44 nf=1 ad='int((nf+1)/2) * W/nf * 0.29'
+ as='int((nf+2)/2) * W/nf * 0.29' pd='2*int((nf+1)/2) * (W/nf + 0.29)' ps='2*int((nf+2)/2) * (W/nf + 0.29)'
+ nrd='0.29 / W' nrs='0.29 / W' sa=0 sb=0 sd=0 mult=5 m=5
XMNClkin_b2 net1 Clkb_int GND GND sky130_fd_pr__nfet_01v8 L=0.15 W=0.84 nf=1 ad='int((nf+1)/2) * W/nf * 0.29'
+ as='int((nf+2)/2) * W/nf * 0.29' pd='2*int((nf+1)/2) * (W/nf + 0.29)' ps='2*int((nf+2)/2) * (W/nf + 0.29)'
+ nrd='0.29 / W' nrs='0.29 / W' sa=0 sb=0 sd=0 mult=3 m=3
XMPClkin_b1 Clkb_int Clk_In VDD VDD sky130_fd_pr__pfet_01v8 L=0.15 W=1.44 nf=1 ad='int((nf+1)/2) * W/nf * 0.29'
+ as='int((nf+2)/2) * W/nf * 0.29' pd='2*int((nf+1)/2) * (W/nf + 0.29)' ps='2*int((nf+2)/2) * (W/nf + 0.29)'
+ nrd='0.29 / W' nrs='0.29 / W' sa=0 sb=0 sd=0 mult=2 m=2
XMNClkin_b1 Clkb_int Clk_In GND GND sky130_fd_pr__nfet_01v8 L=0.15 W=0.84 nf=1 ad='int((nf+1)/2) * W/nf * 0.29'
+ as='int((nf+2)/2) * W/nf * 0.29' pd='2*int((nf+1)/2) * (W/nf + 0.29)' ps='2*int((nf+2)/2) * (W/nf + 0.29)'
+ nrd='0.29 / W' nrs='0.29 / W' sa=0 sb=0 sd=0 mult=2 m=2
XMPClkin_b3 Clkb_buf net1 VDD VDD sky130_fd_pr__pfet_01v8 L=0.15 W=1.44 nf=1 ad='int((nf+1)/2) * W/nf * 0.29'
+ as='int((nf+2)/2) * W/nf * 0.29' pd='2*int((nf+1)/2) * (W/nf + 0.29)' ps='2*int((nf+2)/2) * (W/nf + 0.29)'
+ nrd='0.29 / W' nrs='0.29 / W' sa=0 sb=0 sd=0 mult=7 m=7
XMNClkin_b3 Clkb_buf net1 GND GND sky130_fd_pr__nfet_01v8 L=0.15 W=0.84 nf=1 ad='int((nf+1)/2) * W/nf * 0.29'
+ as='int((nf+2)/2) * W/nf * 0.29' pd='2*int((nf+1)/2) * (W/nf + 0.29)' ps='2*int((nf+2)/2) * (W/nf + 0.29)'
+ nrd='0.29 / W' nrs='0.29 / W' sa=0 sb=0 sd=0 mult=5 m=5
.ends


* expanding   symbol:  FD.sym # of pins=4
** sym_path: xschem/3-stage_cs-vco_dp9/FD.sym
** sch_path: xschem/3-stage_cs-vco_dp9/FD.sch
.subckt FD VDD Clk_Out GND Clk_In
*.ipin Clk_In
*.iopin VDD
*.iopin GND
*.opin Clk_Out
XM15 7 6 VDD VDD sky130_fd_pr__pfet_01v8 L=0.15 W=0.72 nf=1 ad='int((nf+1)/2) * W/nf * 0.29' as='int((nf+2)/2) * W/nf * 0.29'
+ pd='2*int((nf+1)/2) * (W/nf + 0.29)' ps='2*int((nf+2)/2) * (W/nf + 0.29)' nrd='0.29 / W' nrs='0.29 / W'
+ sa=0 sb=0 sd=0 mult=1 m=1
XM16 7 6 GND GND sky130_fd_pr__nfet_01v8 L=0.15 W=0.42 nf=1 ad='int((nf+1)/2) * W/nf * 0.29' as='int((nf+2)/2) * W/nf * 0.29'
+ pd='2*int((nf+1)/2) * (W/nf + 0.29)' ps='2*int((nf+2)/2) * (W/nf + 0.29)' nrd='0.29 / W' nrs='0.29 / W'
+ sa=0 sb=0 sd=0 mult=1 m=1
XM11 2 6 VDD VDD sky130_fd_pr__pfet_01v8 L=0.15 W=0.72 nf=1 ad='int((nf+1)/2) * W/nf * 0.29' as='int((nf+2)/2) * W/nf * 0.29'
+ pd='2*int((nf+1)/2) * (W/nf + 0.29)' ps='2*int((nf+2)/2) * (W/nf + 0.29)' nrd='0.29 / W' nrs='0.29 / W'
+ sa=0 sb=0 sd=0 mult=1 m=1
XM12 2 6 GND GND sky130_fd_pr__nfet_01v8 L=0.15 W=0.42 nf=1 ad='int((nf+1)/2) * W/nf * 0.29' as='int((nf+2)/2) * W/nf * 0.29'
+ pd='2*int((nf+1)/2) * (W/nf + 0.29)' ps='2*int((nf+2)/2) * (W/nf + 0.29)' nrd='0.29 / W' nrs='0.29 / W'
+ sa=0 sb=0 sd=0 mult=1 m=1
XM13 Clkb Clk_In VDD VDD sky130_fd_pr__pfet_01v8 L=0.15 W=0.72 nf=1 ad='int((nf+1)/2) * W/nf * 0.29'
+ as='int((nf+2)/2) * W/nf * 0.29' pd='2*int((nf+1)/2) * (W/nf + 0.29)' ps='2*int((nf+2)/2) * (W/nf + 0.29)'
+ nrd='0.29 / W' nrs='0.29 / W' sa=0 sb=0 sd=0 mult=1 m=1
XM14 Clkb Clk_In GND GND sky130_fd_pr__nfet_01v8 L=0.15 W=0.42 nf=1 ad='int((nf+1)/2) * W/nf * 0.29'
+ as='int((nf+2)/2) * W/nf * 0.29' pd='2*int((nf+1)/2) * (W/nf + 0.29)' ps='2*int((nf+2)/2) * (W/nf + 0.29)'
+ nrd='0.29 / W' nrs='0.29 / W' sa=0 sb=0 sd=0 mult=1 m=1
XM7 5 4 VDD VDD sky130_fd_pr__pfet_01v8 L=0.15 W=0.72 nf=1 ad='int((nf+1)/2) * W/nf * 0.29' as='int((nf+2)/2) * W/nf * 0.29'
+ pd='2*int((nf+1)/2) * (W/nf + 0.29)' ps='2*int((nf+2)/2) * (W/nf + 0.29)' nrd='0.29 / W' nrs='0.29 / W'
+ sa=0 sb=0 sd=0 mult=1 m=1
XM8 5 4 GND GND sky130_fd_pr__nfet_01v8 L=0.15 W=0.42 nf=1 ad='int((nf+1)/2) * W/nf * 0.29' as='int((nf+2)/2) * W/nf * 0.29'
+ pd='2*int((nf+1)/2) * (W/nf + 0.29)' ps='2*int((nf+2)/2) * (W/nf + 0.29)' nrd='0.29 / W' nrs='0.29 / W'
+ sa=0 sb=0 sd=0 mult=1 m=1
XM1 3 2 VDD VDD sky130_fd_pr__pfet_01v8 L=0.15 W=0.72 nf=1 ad='int((nf+1)/2) * W/nf * 0.29' as='int((nf+2)/2) * W/nf * 0.29'
+ pd='2*int((nf+1)/2) * (W/nf + 0.29)' ps='2*int((nf+2)/2) * (W/nf + 0.29)' nrd='0.29 / W' nrs='0.29 / W'
+ sa=0 sb=0 sd=0 mult=1 m=1
XM2 3 2 GND GND sky130_fd_pr__nfet_01v8 L=0.15 W=0.42 nf=1 ad='int((nf+1)/2) * W/nf * 0.29' as='int((nf+2)/2) * W/nf * 0.29'
+ pd='2*int((nf+1)/2) * (W/nf + 0.29)' ps='2*int((nf+2)/2) * (W/nf + 0.29)' nrd='0.29 / W' nrs='0.29 / W'
+ sa=0 sb=0 sd=0 mult=1 m=1
XM3 4 Clkb 3 VDD sky130_fd_pr__pfet_01v8 L=0.15 W=0.42 nf=1 ad='int((nf+1)/2) * W/nf * 0.29' as='int((nf+2)/2) * W/nf * 0.29'
+ pd='2*int((nf+1)/2) * (W/nf + 0.29)' ps='2*int((nf+2)/2) * (W/nf + 0.29)' nrd='0.29 / W' nrs='0.29 / W'
+ sa=0 sb=0 sd=0 mult=1 m=1
XM4 4 Clk_In 3 GND sky130_fd_pr__nfet_01v8 L=0.15 W=0.84 nf=1 ad='int((nf+1)/2) * W/nf * 0.29' as='int((nf+2)/2) * W/nf * 0.29'
+ pd='2*int((nf+1)/2) * (W/nf + 0.29)' ps='2*int((nf+2)/2) * (W/nf + 0.29)' nrd='0.29 / W' nrs='0.29 / W'
+ sa=0 sb=0 sd=0 mult=1 m=1
XM9 6 Clk_In 5 VDD sky130_fd_pr__pfet_01v8 L=0.15 W=0.42 nf=1 ad='int((nf+1)/2) * W/nf * 0.29' as='int((nf+2)/2) * W/nf * 0.29'
+ pd='2*int((nf+1)/2) * (W/nf + 0.29)' ps='2*int((nf+2)/2) * (W/nf + 0.29)' nrd='0.29 / W' nrs='0.29 / W'
+ sa=0 sb=0 sd=0 mult=1 m=1
XM10 6 Clkb 5 GND sky130_fd_pr__nfet_01v8 L=0.15 W=0.84 nf=1 ad='int((nf+1)/2) * W/nf * 0.29' as='int((nf+2)/2) * W/nf * 0.29'
+ pd='2*int((nf+1)/2) * (W/nf + 0.29)' ps='2*int((nf+2)/2) * (W/nf + 0.29)' nrd='0.29 / W' nrs='0.29 / W'
+ sa=0 sb=0 sd=0 mult=1 m=1
XM19 Clk_Out 7 VDD VDD sky130_fd_pr__pfet_01v8 L=0.15 W=0.72 nf=1 ad='int((nf+1)/2) * W/nf * 0.29' as='int((nf+2)/2) * W/nf * 0.29'
+ pd='2*int((nf+1)/2) * (W/nf + 0.29)' ps='2*int((nf+2)/2) * (W/nf + 0.29)' nrd='0.29 / W' nrs='0.29 / W'
+ sa=0 sb=0 sd=0 mult=1 m=1
XM20 Clk_Out 7 GND GND sky130_fd_pr__nfet_01v8 L=0.15 W=0.42 nf=1 ad='int((nf+1)/2) * W/nf * 0.29' as='int((nf+2)/2) * W/nf * 0.29'
+ pd='2*int((nf+1)/2) * (W/nf + 0.29)' ps='2*int((nf+2)/2) * (W/nf + 0.29)' nrd='0.29 / W' nrs='0.29 / W'
+ sa=0 sb=0 sd=0 mult=1 m=1
.ends


* expanding   symbol:  vco_switch_n.sym # of pins=5
** sym_path: xschem/3-stage_cs-vco_dp9/vco_switch_n.sym
** sch_path: xschem/3-stage_cs-vco_dp9/vco_switch_n.sch
.subckt vco_switch_n vdd out in vss sel
*.ipin in
*.ipin sel
*.opin out
*.iopin vss
*.iopin vdd
XM26 in sel out vss sky130_fd_pr__nfet_01v8 L=0.18 W=0.42 nf=1 ad='int((nf+1)/2) * W/nf * 0.29' as='int((nf+2)/2) * W/nf * 0.29'
+ pd='2*int((nf+1)/2) * (W/nf + 0.29)' ps='2*int((nf+2)/2) * (W/nf + 0.29)' nrd='0.29 / W' nrs='0.29 / W'
+ sa=0 sb=0 sd=0 mult=1 m=1
XM25 out selb in vdd sky130_fd_pr__pfet_01v8 L=0.18 W=0.72 nf=1 ad='int((nf+1)/2) * W/nf * 0.29' as='int((nf+2)/2) * W/nf * 0.29'
+ pd='2*int((nf+1)/2) * (W/nf + 0.29)' ps='2*int((nf+2)/2) * (W/nf + 0.29)' nrd='0.29 / W' nrs='0.29 / W'
+ sa=0 sb=0 sd=0 mult=1 m=1
XM1 out selb vss vss sky130_fd_pr__nfet_01v8 L=0.18 W=0.42 nf=1 ad='int((nf+1)/2) * W/nf * 0.29' as='int((nf+2)/2) * W/nf * 0.29'
+ pd='2*int((nf+1)/2) * (W/nf + 0.29)' ps='2*int((nf+2)/2) * (W/nf + 0.29)' nrd='0.29 / W' nrs='0.29 / W'
+ sa=0 sb=0 sd=0 mult=1 m=1
x1 sel vss vss vdd vdd selb sky130_fd_sc_hd__inv_1
**** begin user architecture code

.include /usr/local/share/pdk/sky130A/libs.ref/sky130_fd_sc_hd/spice/sky130_fd_sc_hd.spice

**** end user architecture code
.ends


* expanding   symbol:  vco_switch_p.sym # of pins=5
** sym_path: xschem/3-stage_cs-vco_dp9/vco_switch_p.sym
** sch_path: xschem/3-stage_cs-vco_dp9/vco_switch_p.sch
.subckt vco_switch_p vdd out in vss sel
*.ipin in
*.ipin sel
*.opin out
*.iopin vss
*.iopin vdd
XM26 in sel out vss sky130_fd_pr__nfet_01v8 L=0.18 W=0.42 nf=1 ad='int((nf+1)/2) * W/nf * 0.29' as='int((nf+2)/2) * W/nf * 0.29'
+ pd='2*int((nf+1)/2) * (W/nf + 0.29)' ps='2*int((nf+2)/2) * (W/nf + 0.29)' nrd='0.29 / W' nrs='0.29 / W'
+ sa=0 sb=0 sd=0 mult=1 m=1
XM25 out selb in vdd sky130_fd_pr__pfet_01v8 L=0.18 W=0.72 nf=1 ad='int((nf+1)/2) * W/nf * 0.29' as='int((nf+2)/2) * W/nf * 0.29'
+ pd='2*int((nf+1)/2) * (W/nf + 0.29)' ps='2*int((nf+2)/2) * (W/nf + 0.29)' nrd='0.29 / W' nrs='0.29 / W'
+ sa=0 sb=0 sd=0 mult=1 m=1
x1 sel vss vss vdd vdd selb sky130_fd_sc_hd__inv_1
XM1 vdd sel out vdd sky130_fd_pr__pfet_01v8 L=0.18 W=0.72 nf=1 ad='int((nf+1)/2) * W/nf * 0.29' as='int((nf+2)/2) * W/nf * 0.29'
+ pd='2*int((nf+1)/2) * (W/nf + 0.29)' ps='2*int((nf+2)/2) * (W/nf + 0.29)' nrd='0.29 / W' nrs='0.29 / W'
+ sa=0 sb=0 sd=0 mult=1 m=1
**** begin user architecture code

.include /usr/local/share/pdk/sky130A/libs.ref/sky130_fd_sc_hd/spice/sky130_fd_sc_hd.spice

**** end user architecture code
.ends

.end
